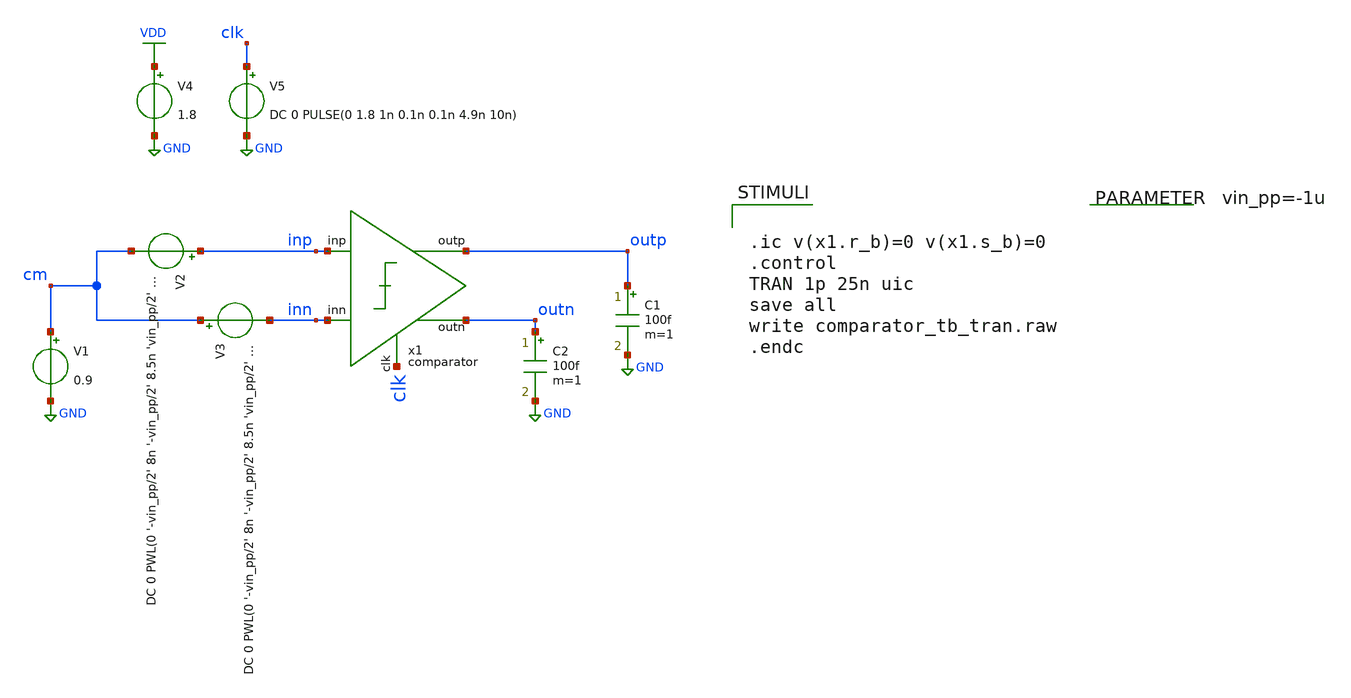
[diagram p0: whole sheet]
** sch_path: verification/schematic/comparator_tb_tran.sch
**.subckt comparator_tb_tran
x1 inp inn outp clk outn VDD GND comparator
V1 cm GND 0.9
V4 VDD GND 1.8
V5 clk GND DC 0 PULSE(0 1.8 1n 0.1n 0.1n 4.9n 10n)
C1 outp GND 100f m=1
.param vin_pp=-1u
C2 outn GND 100f m=1
V2 inp cm DC 0 PWL(0 '-vin_pp/2' 8n '-vin_pp/2' 8.5n 'vin_pp/2' 18n 'vin_pp/2' 18.5n '-vin_pp/2')
V3 cm inn DC 0 PWL(0 '-vin_pp/2' 8n '-vin_pp/2' 8.5n 'vin_pp/2' 18n 'vin_pp/2' 18.5n '-vin_pp/2')
**** begin user architecture code

** opencircuitdesign pdks install
.lib /farmshare/home/classes/ee/372/PDKs/open_pdks_1.0.310/sky130/sky130A/libs.tech/ngspice/sky130.lib.spice tt
.inc /farmshare/home/classes/ee/372/PDKs/open_pdks_1.0.310/sky130/sky130A/libs.ref/sky130_fd_sc_hd/spice/sky130_fd_sc_hd.spice



.ic v(x1.r_b)=0 v(x1.s_b)=0
.control
TRAN 1p 25n uic
save all
write comparator_tb_tran.raw
.endc



**** end user architecture code
**.ends
.GLOBAL GND
.GLOBAL VDD
.end
